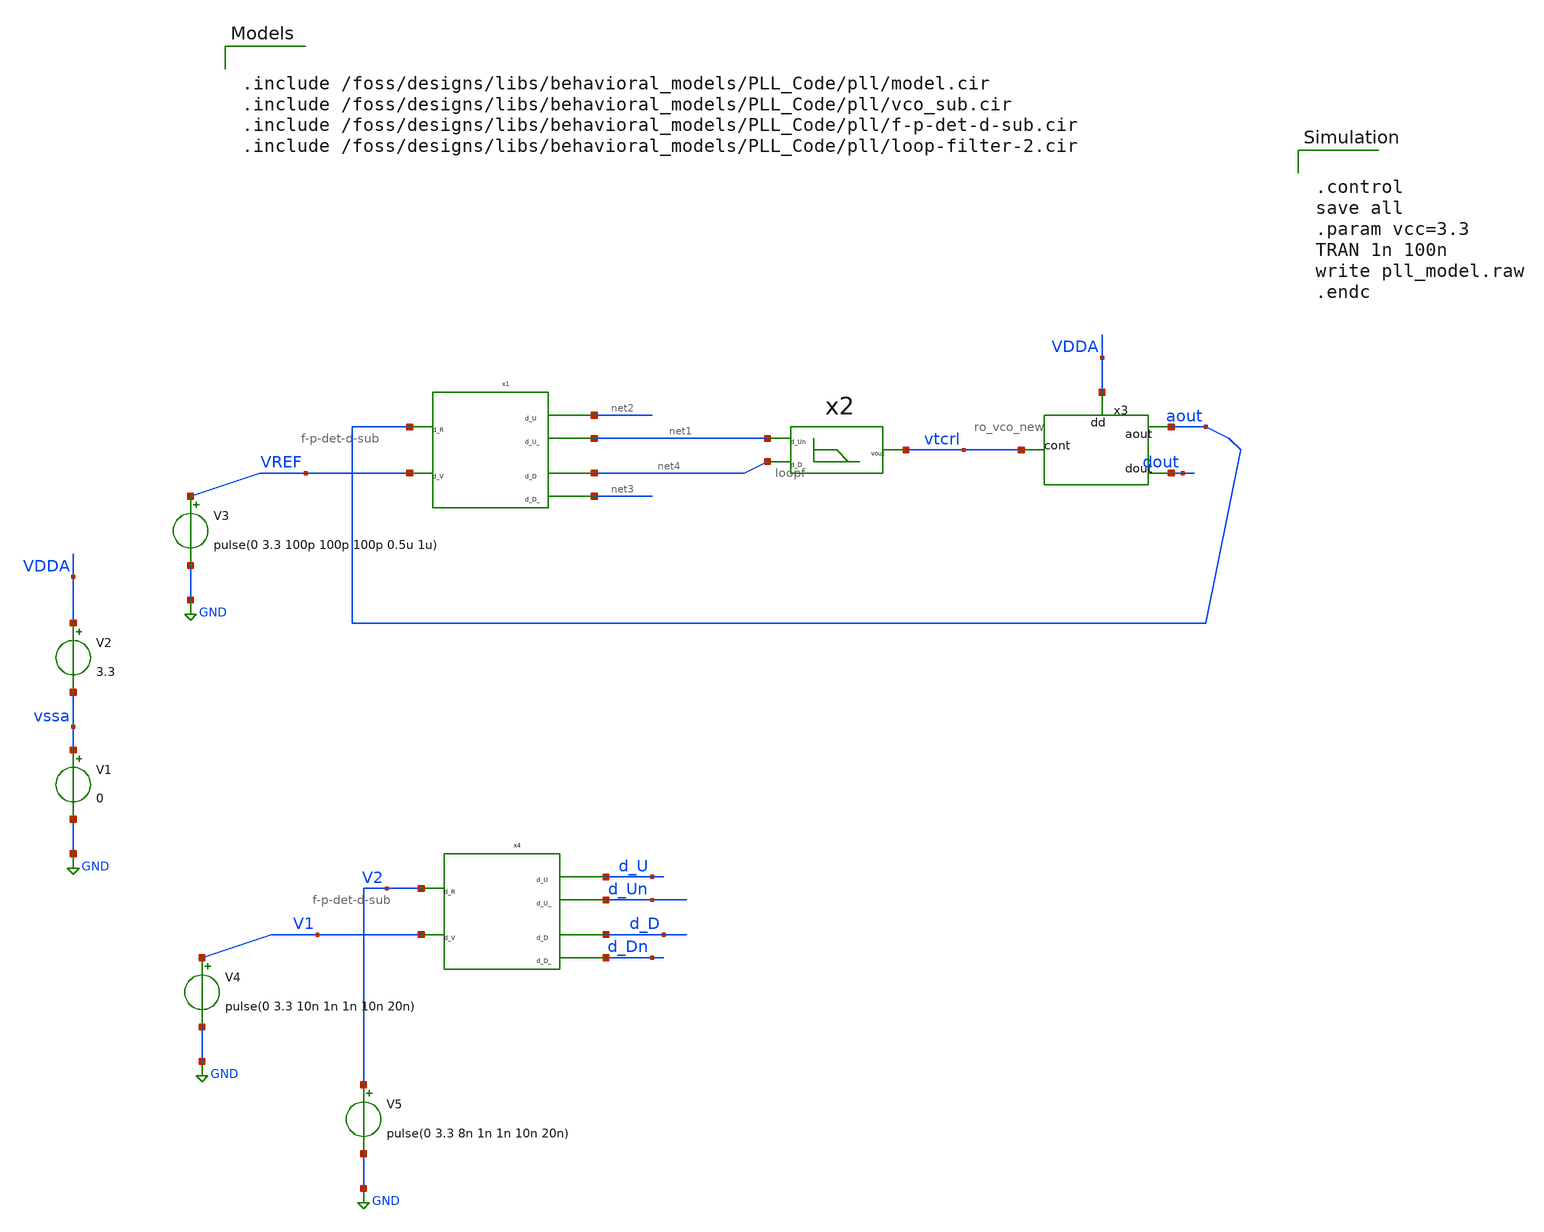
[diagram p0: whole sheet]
** sch_path: designs/libs/tb_analog/tb_PLL_behavioral_models/tb_pll_behaviour.sch
**.subckt tb_pll_behaviour
x1 aout VREF net2 net1 net4 net3 f-p-det-d-sub
x2 net1 net4 vtcrl loopf
x3 aout dout vtcrl VDDA ro_vco_new
V1 vssa GND 0
V3 VREF GND pulse(0 3.3 100p 100p 100p 0.5u 1u)
V2 VDDA vssa 3.3
x4 V2 V1 d_U d_Un d_D d_Dn f-p-det-d-sub
V4 V1 GND pulse(0 3.3 10n 1n 1n 10n 20n)
V5 V2 GND pulse(0 3.3 8n 1n 1n 10n 20n)
**** begin user architecture code

.include /foss/designs/libs/behavioral_models/PLL_Code/pll/model.cir
.include /foss/designs/libs/behavioral_models/PLL_Code/pll/vco_sub.cir
.include /foss/designs/libs/behavioral_models/PLL_Code/pll/f-p-det-d-sub.cir
.include /foss/designs/libs/behavioral_models/PLL_Code/pll/loop-filter-2.cir



.control
save all
.param vcc=3.3
TRAN 1n 100n
write pll_model.raw
.endc


**** end user architecture code
**.ends
.GLOBAL GND
.end
